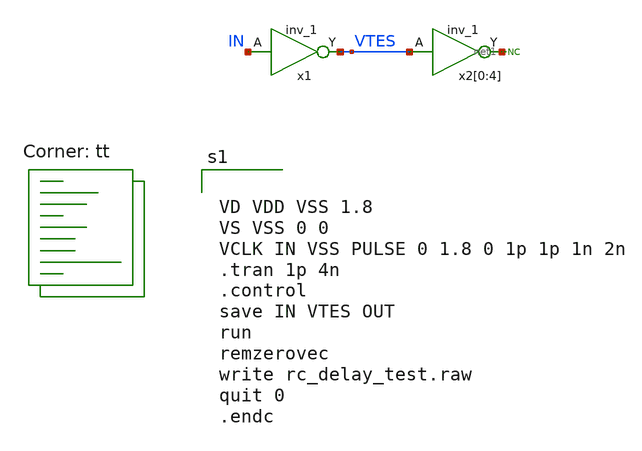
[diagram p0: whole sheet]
** sch_path: xschem/rc_delay_test.sch
**.subckt rc_delay_test
x1 IN VSS VSS VDD VDD VTES sky130_fd_sc_hs__inv_1
x2[0] VTES VSS VSS VDD VDD net1[4] sky130_fd_sc_hs__inv_1
x2[1] VTES VSS VSS VDD VDD net1[3] sky130_fd_sc_hs__inv_1
x2[2] VTES VSS VSS VDD VDD net1[2] sky130_fd_sc_hs__inv_1
x2[3] VTES VSS VSS VDD VDD net1[1] sky130_fd_sc_hs__inv_1
x2[4] VTES VSS VSS VDD VDD net1[0] sky130_fd_sc_hs__inv_1
* noconn #net1
**** begin user architecture code

** opencircuitdesign pdks install
* .lib $::SKYWATER_MODELS/sky130.lib.spice tt
*.include $PDK_ROOT/$PDK/libs.ref/sky130_fd_sc_hdll/spice/sky130_fd_sc_hdll.spice
.include $PDK_ROOT/$PDK/libs.ref/sky130_fd_sc_hs/spice/sky130_fd_sc_hs.spice
*.include $PDK_ROOT/$PDK/libs.ref/sky130_fd_sc_hd/spice/sky130_fd_sc_hd.spice

.lib $::SKYWATER_MODELS/sky130.lib.spice tt


VD VDD VSS 1.8
VS VSS 0 0
VCLK IN VSS PULSE 0 1.8 0 1p 1p 1n 2n
.tran 1p 4n
.control
save IN VTES OUT
run
remzerovec
write rc_delay_test.raw
quit 0
.endc


**** end user architecture code
**.ends
.end
